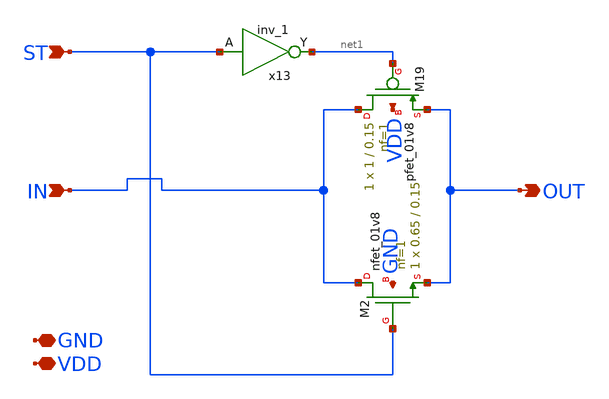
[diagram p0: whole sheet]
** sch_path: design/xschem/tranmission_gate_fc.sch
**.subckt tranmission_gate_fc GND VDD ST IN OUT
*.iopin GND
*.iopin VDD
*.ipin ST
*.ipin IN
*.opin OUT
x13 ST GND GND VDD VDD net1 sky130_fd_sc_hd__inv_1
XM19 IN net1 OUT VDD sky130_fd_pr__pfet_01v8 L=0.15 W=1 nf=1 ad='int((nf+1)/2) * W/nf * 0.29' as='int((nf+2)/2) * W/nf * 0.29'
+ pd='2*int((nf+1)/2) * (W/nf + 0.29)' ps='2*int((nf+2)/2) * (W/nf + 0.29)' nrd='0.29 / W' nrs='0.29 / W'
+ sa=0 sb=0 sd=0 mult=1 m=1
XM2 IN ST OUT GND sky130_fd_pr__nfet_01v8 L=0.15 W=0.65 nf=1 ad='int((nf+1)/2) * W/nf * 0.29' as='int((nf+2)/2) * W/nf * 0.29'
+ pd='2*int((nf+1)/2) * (W/nf + 0.29)' ps='2*int((nf+2)/2) * (W/nf + 0.29)' nrd='0.29 / W' nrs='0.29 / W'
+ sa=0 sb=0 sd=0 mult=1 m=1
**.ends
.end
